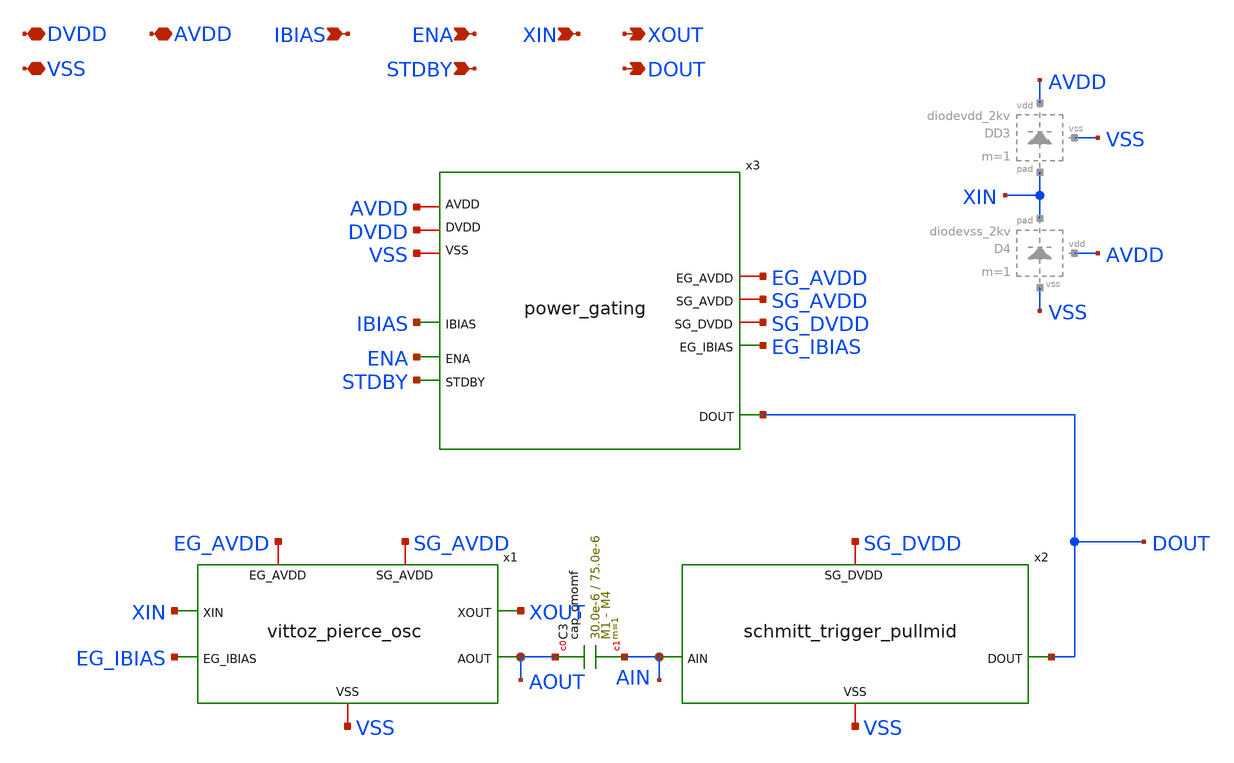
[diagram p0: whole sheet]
** sch_path: xschem/sg13cmos5l_ht_ip__hsxo_cpz2.sch
**.subckt sg13cmos5l_ht_ip__hsxo_cpz2 DVDD VSS AVDD ENA STDBY XIN XOUT DOUT IBIAS
*.iopin DVDD
*.iopin VSS
*.iopin AVDD
*.ipin ENA
*.ipin STDBY
*.ipin XIN
*.opin XOUT
*.opin DOUT
*.ipin IBIAS
x1 XOUT SG_AVDD EG_AVDD XIN EG_IBIAS AOUT VSS vittoz_pierce_osc
x2 SG_DVDD AIN DOUT VSS schmitt_trigger_pullmid
x3 DOUT SG_AVDD DVDD EG_IBIAS SG_DVDD AVDD IBIAS EG_AVDD ENA STDBY VSS power_gating
XC3 AOUT AIN cap_cmomf w=30.0e-6 l=75.0e-6 mmin=1 mmax=4 subblock=0 rfmodel=0 subscale=1 m=1 mm_ok=1
**.ends

* expanding   symbol:  vittoz_pierce_osc.sym # of pins=7
** sym_path: xschem/vittoz_pierce_osc.sym
** sch_path: xschem/vittoz_pierce_osc.sch
.subckt vittoz_pierce_osc XOUT SG_AVDD EG_AVDD XIN EG_IBIAS AOUT VSS
*.iopin EG_AVDD
*.iopin VSS
*.iopin SG_AVDD
*.ipin XIN
*.ipin EG_IBIAS
*.opin XOUT
*.opin AOUT
Vmeas3 net6 XOUT 0
.save i(vmeas3)
Vmeas4 net7 net1 0
.save i(vmeas4)
Vmeas2 PBIAS net3 0
.save i(vmeas2)
Vmeas5 net8 AOUT 0
.save i(vmeas5)
Vmeas1 EG_IBIAS net4 0
.save i(vmeas1)
XC3 VSS EG_AVDD cap_cmomf w=30.0e-6 l=75.0e-6 mmin=1 mmax=4 subblock=0 rfmodel=0 subscale=1 m=1
+ mm_ok=1
XC4 VSS SG_AVDD cap_cmomf w=30.0e-6 l=75.0e-6 mmin=1 mmax=4 subblock=0 rfmodel=0 subscale=1 m=1
+ mm_ok=1
XR1 net1 net2 VSS rhigh w=0.5e-6 l=1.342e-5 m=1 b=0 mm_ok=1
XR2 XOUT XIN VSS rhigh w=0.5e-6 l=5.305e-6 m=1 b=0 mm_ok=1
XC2 XIN net2 cap_cmomf w=30.0e-6 l=75.0e-6 mmin=1 mmax=4 subblock=0 rfmodel=0 subscale=1 m=1 mm_ok=1
XC7 net2 VSS cap_cmomf w=30.0e-6 l=75.0e-6 mmin=1 mmax=4 subblock=0 rfmodel=0 subscale=1 m=1 mm_ok=1
XC1 VSS net1 cap_cmomf w=4.0e-6 l=4.0e-6 mmin=1 mmax=1 subblock=0 rfmodel=0 subscale=1 m=1 mm_ok=1
XC8 VSS AOUT cap_cmomf w=4.0e-6 l=4.0e-6 mmin=1 mmax=1 subblock=0 rfmodel=0 subscale=1 m=1 mm_ok=1
XM11 PBIAS PBIAS EG_AVDD EG_AVDD sg13_hv_pmos w=102.4u l=0.4u ng=16 m=1 mm_ok=1
XM10 net7 PBIAS EG_AVDD EG_AVDD sg13_hv_pmos w=102.4u l=0.4u ng=16 m=1 mm_ok=1
XM9 net6 PBIAS EG_AVDD EG_AVDD sg13_hv_pmos w=819.2u l=0.4u ng=128 m=1 mm_ok=1
XM14 net3 net2 net5 VSS sg13_hv_nmos w=921.6u l=0.45u ng=128 m=1 mm_ok=1
XM12 net1 net2 VSS VSS sg13_hv_nmos w=115.2u l=0.45u ng=16 m=1 mm_ok=1
XM13 XOUT XIN VSS VSS sg13_hv_nmos w=28.8u l=0.45u ng=32 m=1 mm_ok=1
XM15 net5 net4 VSS VSS sg13_hv_nmos w=115.2u l=0.45u ng=16 m=1 mm_ok=1
XM16 net4 net4 VSS VSS sg13_hv_nmos w=7.2u l=0.45u ng=4 m=1 mm_ok=1
XM18 net8 PBIAS SG_AVDD SG_AVDD sg13_hv_pmos w=102.4u l=0.4u ng=16 m=1 mm_ok=1
XM17 AOUT XIN VSS VSS sg13_hv_nmos w=3.6u l=0.45u ng=4 m=1 mm_ok=1
.ends


* expanding   symbol:  schmitt_trigger_pullmid.sym # of pins=4
** sym_path: xschem/schmitt_trigger_pullmid.sym
** sch_path: xschem/schmitt_trigger_pullmid.sch
.subckt schmitt_trigger_pullmid SG_DVDD AIN DOUT VSS
*.iopin SG_DVDD
*.iopin VSS
*.ipin AIN
*.opin DOUT
Vmeas6 AIN net1 0
.save i(vmeas6)
XR1 SG_DVDD MID VSS rhigh w=0.5e-6 l=3.1e-5 m=1 b=0 mm_ok=1
XR2 MID VSS VSS rhigh w=0.5e-6 l=3.1e-5 m=1 b=0 mm_ok=1
XR3 net1 MID VSS rhigh w=0.5e-6 l=2.5e-4 m=1 b=0 mm_ok=1
XC4 VSS SG_DVDD cap_cmomf w=30.0e-6 l=75.0e-6 mmin=1 mmax=4 subblock=0 rfmodel=0 subscale=1 m=1
+ mm_ok=1
XM4 DOUT net1 DLT VSS sg13_lv_nmos w=1u l=0.3u ng=1 m=1 mm_ok=1
XM5 DHT net1 SG_DVDD SG_DVDD sg13_lv_pmos w=1u l=0.3u ng=1 m=1 mm_ok=1
XM3 DOUT net1 DHT SG_DVDD sg13_lv_pmos w=1u l=0.3u ng=1 m=1 mm_ok=1
XM7 VSS DOUT DHT SG_DVDD sg13_lv_pmos w=1u l=0.3u ng=1 m=1 mm_ok=1
XM6 DLT net1 VSS VSS sg13_lv_nmos w=1u l=0.3u ng=1 m=1 mm_ok=1
XM8 SG_DVDD DOUT DLT VSS sg13_lv_nmos w=1u l=0.3u ng=1 m=1 mm_ok=1
.ends


* expanding   symbol:  power_gating.sym # of pins=11
** sym_path: xschem/power_gating.sym
** sch_path: xschem/power_gating.sch
.subckt power_gating DOUT SG_AVDD DVDD EG_IBIAS SG_DVDD AVDD IBIAS EG_AVDD ENA STDBY VSS
*.iopin DVDD
*.iopin VSS
*.iopin AVDD
*.ipin ENA
*.ipin STDBY
*.opin DOUT
*.ipin IBIAS
*.iopin EG_AVDD
*.iopin SG_AVDD
*.iopin SG_DVDD
*.opin EG_IBIAS
x3 AVDD ENA_B DVDD ENA ENA_H VSS ENA_BH level_shifter
x4 AVDD STDBY_B DVDD STDBY STDBY_H VSS STDBY_BH level_shifter
XC3 VSS AVDD cap_cmomf w=30.0e-6 l=75.0e-6 mmin=1 mmax=4 subblock=0 rfmodel=0 subscale=1 m=1 mm_ok=1
XC4 VSS DVDD cap_cmomf w=30.0e-6 l=75.0e-6 mmin=1 mmax=4 subblock=0 rfmodel=0 subscale=1 m=1 mm_ok=1
XM2 EG_IBIAS ENA_BH net1 AVDD sg13_hv_pmos w=25.6u l=0.4u ng=8 m=1 mm_ok=1
XM1 SG_AVDD STDBY_H AVDD AVDD sg13_hv_pmos w=25.6u l=0.4u ng=8 m=1 mm_ok=1
XM25 EG_AVDD ENA_BH AVDD AVDD sg13_hv_pmos w=25.6u l=0.4u ng=8 m=1 mm_ok=1
XM9 SG_AVDD STDBY_H VSS VSS sg13_hv_nmos w=28.8u l=0.45u ng=8 m=1 mm_ok=1
XM21 EG_AVDD ENA_BH VSS VSS sg13_hv_nmos w=28.8u l=0.45u ng=8 m=1 mm_ok=1
XM27 SG_DVDD STDBY DVDD DVDD sg13_lv_pmos w=27.73u l=0.13u ng=8 m=1 mm_ok=1
XM18 SG_DVDD STDBY VSS VSS sg13_lv_nmos w=27.73u l=0.13u ng=8 m=1 mm_ok=1
XM4 DOUT STDBY VSS VSS sg13_lv_nmos w=27.73u l=0.13u ng=8 m=1 mm_ok=1
Vmeas1 IBIAS net1 0
.save i(vmeas1)
Vmeas2 IBIAS net2 0
.save i(vmeas2)
XM3 VSS ENA_H net2 AVDD sg13_hv_pmos w=25.6u l=0.4u ng=8 m=1 mm_ok=1
.ends


* expanding   symbol:  level_shifter.sym # of pins=7
** sym_path: xschem/level_shifter.sym
** sch_path: xschem/level_shifter.sch
.subckt level_shifter AVDD LO_B DVDD LO HI VSS HI_B
*.iopin DVDD
*.iopin VSS
*.iopin AVDD
*.ipin LO
*.opin LO_B
*.opin HI
*.opin HI_B
XM1 IM_B IM AVDD AVDD sg13_hv_pmos w=0.8u l=0.4u ng=1 m=1 mm_ok=1
XM2 IM_B LO_BB VSS VSS sg13_hv_nmos w=0.9u l=0.45u ng=1 m=1 mm_ok=1
XM3 IM IM_B AVDD AVDD sg13_hv_pmos w=0.8u l=0.4u ng=1 m=1 mm_ok=1
XM4 IM LO_B VSS VSS sg13_hv_nmos w=0.9u l=0.45u ng=1 m=1 mm_ok=1
XM5 LO_B LO DVDD DVDD sg13_lv_pmos w=0.87u l=0.13u ng=1 m=1 mm_ok=1
XM6 LO_B LO VSS VSS sg13_lv_nmos w=0.87u l=0.13u ng=1 m=1 mm_ok=1
XM7 LO_BB LO_B DVDD DVDD sg13_lv_pmos w=0.87u l=0.13u ng=1 m=1 mm_ok=1
XM8 LO_BB LO_B VSS VSS sg13_lv_nmos w=0.87u l=0.13u ng=1 m=1 mm_ok=1
XM9 HI IM_B AVDD AVDD sg13_hv_pmos w=0.8u l=0.4u ng=1 m=1 mm_ok=1
XM10 HI IM_B VSS VSS sg13_hv_nmos w=0.9u l=0.45u ng=1 m=1 mm_ok=1
XM11 HI_B HI AVDD AVDD sg13_hv_pmos w=0.8u l=0.4u ng=1 m=1 mm_ok=1
XM12 HI_B HI VSS VSS sg13_hv_nmos w=0.9u l=0.45u ng=1 m=1 mm_ok=1
.ends

.end
